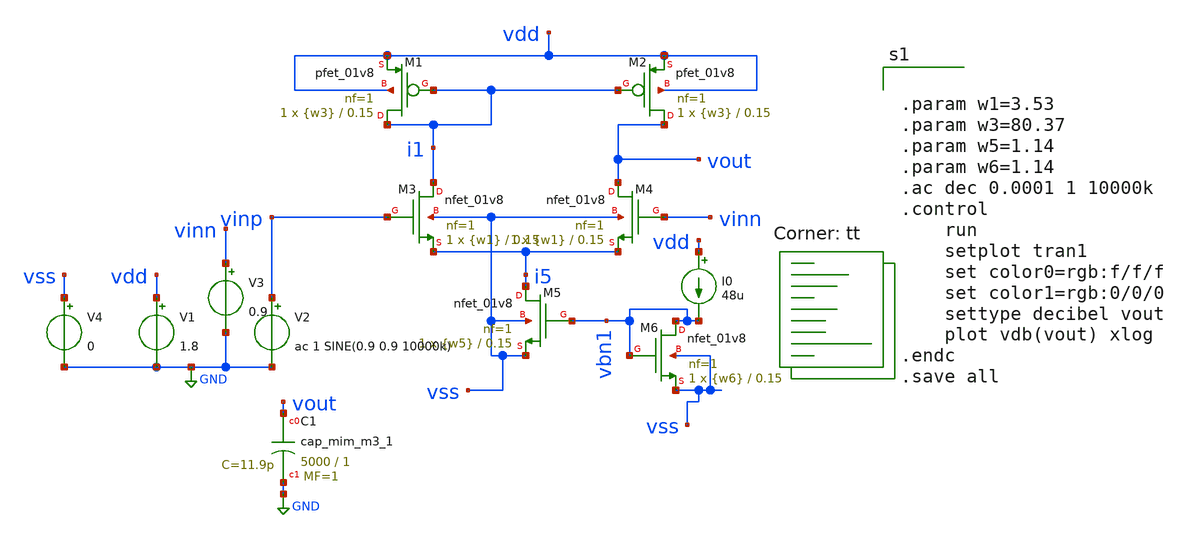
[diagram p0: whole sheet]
** sch_path: opamp_design/opam.sch
**.subckt opam
XM1 i1 i1 vdd vdd sky130_fd_pr__pfet_01v8 L=0.15 W={w3} nf=1 ad='int((nf+1)/2) * W/nf * 0.29' as='int((nf+2)/2) * W/nf * 0.29'
+ pd='2*int((nf+1)/2) * (W/nf + 0.29)' ps='2*int((nf+2)/2) * (W/nf + 0.29)' nrd='0.29 / W' nrs='0.29 / W'
+ sa=0 sb=0 sd=0 mult=1 m=1
XM2 vout i1 vdd vdd sky130_fd_pr__pfet_01v8 L=0.15 W={w3} nf=1 ad='int((nf+1)/2) * W/nf * 0.29' as='int((nf+2)/2) * W/nf * 0.29'
+ pd='2*int((nf+1)/2) * (W/nf + 0.29)' ps='2*int((nf+2)/2) * (W/nf + 0.29)' nrd='0.29 / W' nrs='0.29 / W'
+ sa=0 sb=0 sd=0 mult=1 m=1
XM3 i1 vinp i5 vss sky130_fd_pr__nfet_01v8 L=0.15 W={w1} nf=1 ad='int((nf+1)/2) * W/nf * 0.29' as='int((nf+2)/2) * W/nf * 0.29'
+ pd='2*int((nf+1)/2) * (W/nf + 0.29)' ps='2*int((nf+2)/2) * (W/nf + 0.29)' nrd='0.29 / W' nrs='0.29 / W'
+ sa=0 sb=0 sd=0 mult=1 m=1
XM4 vout vinn i5 vss sky130_fd_pr__nfet_01v8 L=0.15 W={w1} nf=1 ad='int((nf+1)/2) * W/nf * 0.29' as='int((nf+2)/2) * W/nf * 0.29'
+ pd='2*int((nf+1)/2) * (W/nf + 0.29)' ps='2*int((nf+2)/2) * (W/nf + 0.29)' nrd='0.29 / W' nrs='0.29 / W'
+ sa=0 sb=0 sd=0 mult=1 m=1
XM5 i5 vbn1 vss vss sky130_fd_pr__nfet_01v8 L=0.15 W={w5} nf=1 ad='int((nf+1)/2) * W/nf * 0.29' as='int((nf+2)/2) * W/nf * 0.29'
+ pd='2*int((nf+1)/2) * (W/nf + 0.29)' ps='2*int((nf+2)/2) * (W/nf + 0.29)' nrd='0.29 / W' nrs='0.29 / W'
+ sa=0 sb=0 sd=0 mult=1 m=1
XM6 vbn1 vbn1 vss vss sky130_fd_pr__nfet_01v8 L=0.15 W={w6} nf=1 ad='int((nf+1)/2) * W/nf * 0.29' as='int((nf+2)/2) * W/nf * 0.29'
+ pd='2*int((nf+1)/2) * (W/nf + 0.29)' ps='2*int((nf+2)/2) * (W/nf + 0.29)' nrd='0.29 / W' nrs='0.29 / W'
+ sa=0 sb=0 sd=0 mult=1 m=1
I0 vdd vbn1 48u
V1 vdd GND 1.8
V2 vinp GND ac 1 SINE(0.9 0.9 10000k)
V3 vinn GND 0.9
V4 vss GND 0
XC1 vout GND sky130_fd_pr__cap_mim_m3_1 W=5000 L=1 MF=1 m=1
**** begin user architecture code


.param w1=3.53
.param w3=80.37
.param w5=1.14
.param w6=1.14
.ac dec 0.0001 1 10000k
.control
	run
	setplot tran1
	set color0=rgb:f/f/f
	set color1=rgb:0/0/0
	settype decibel vout
	plot vdb(vout) xlog
.endc
.save all


.lib $::SKYWATER_MODELS/sky130.lib.spice tt
**** end user architecture code
**.ends
.GLOBAL GND
.end
